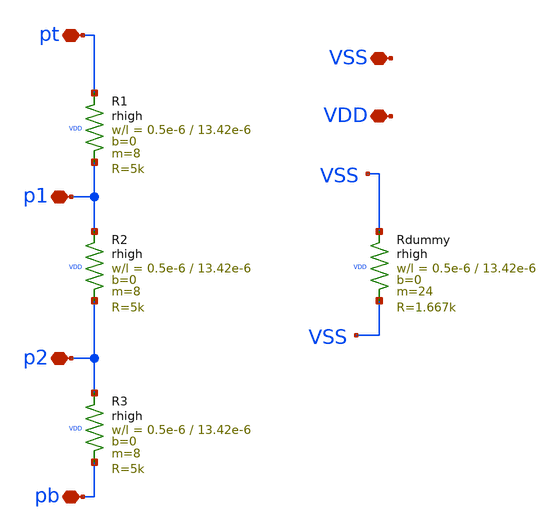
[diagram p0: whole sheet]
** sch_path: macros/resistor_network/schematic/xschem/resistor_leg.sch
**.subckt resistor_leg pt pb p2 p1 VDD VSS
*.iopin pt
*.iopin pb
*.iopin p2
*.iopin p1
*.iopin VDD
*.iopin VSS
XR1 pt p1 VDD rhigh w=0.5e-6 l=13.42e-6 m=8 b=0 mm_ok=1
XR2 p1 p2 VDD rhigh w=0.5e-6 l=13.42e-6 m=8 b=0 mm_ok=1
XR3 p2 pb VDD rhigh w=0.5e-6 l=13.42e-6 m=8 b=0 mm_ok=1
XRdummy VSS VSS VDD rhigh w=0.5e-6 l=13.42e-6 m=24 b=0 mm_ok=1
**.ends
.end
